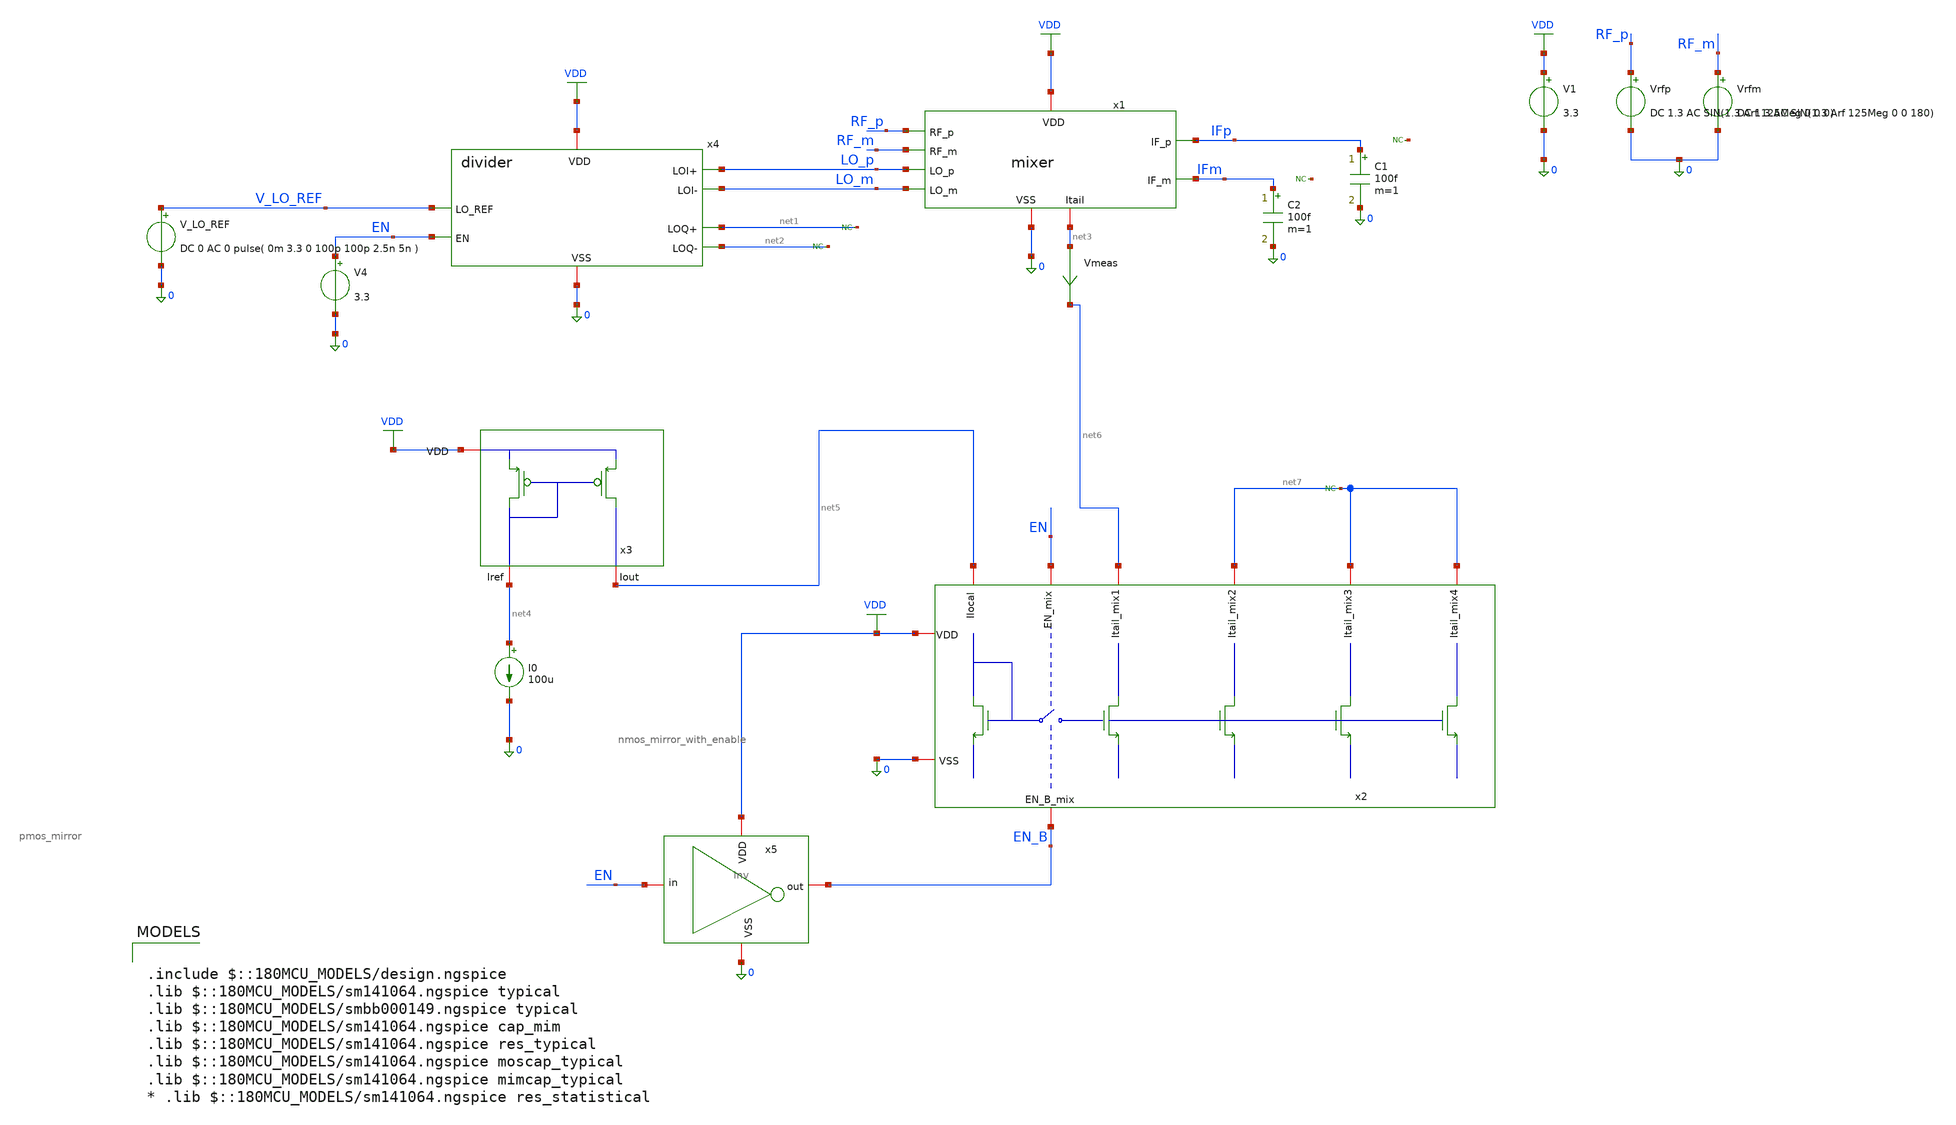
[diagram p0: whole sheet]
** sch_path: designs/mixer/testbench/mixer_p1db.sch
**.subckt mixer_p1db
V1 VDD 0 3.3
Vrfp RF_p 0 DC 1.3 AC SIN(1.3 Arf 125Meg 0 0 0)
Vrfm RF_m 0 DC 1.3 AC SIN(1.3 Arf 125Meg 0 0 180)
C1 IFp 0 100f m=1
C2 IFm 0 100f m=1
x1 IFp RF_p VDD 0 IFm RF_m LO_p net3 LO_m mixer
V_LO_REF V_LO_REF 0 DC 0 AC 0 pulse( 0m 3.3 0 100p 100p 2.5n 5n )
x4 VDD 0 V_LO_REF LO_p LO_m net1 net2 EN divider
* noconn #net1
* noconn #net2
V4 EN 0 3.3
x3 VDD net5 net4 pmos_mirror
I0 net4 0 100u
x2 net7 net7 net5 VDD EN net6 0 EN_B net7 nmos_mirror_with_enable
* noconn #net7
x5 VDD EN_B EN 0 inv
Vmeas net3 net6 0
.save i(vmeas)
* noconn #net8
* noconn #net9
**** begin user architecture code

.include $::180MCU_MODELS/design.ngspice
.lib $::180MCU_MODELS/sm141064.ngspice typical
.lib $::180MCU_MODELS/smbb000149.ngspice typical
.lib $::180MCU_MODELS/sm141064.ngspice cap_mim
.lib $::180MCU_MODELS/sm141064.ngspice res_typical
.lib $::180MCU_MODELS/sm141064.ngspice moscap_typical
.lib $::180MCU_MODELS/sm141064.ngspice mimcap_typical
* .lib $::180MCU_MODELS/sm141064.ngspice res_statistical




.param Arf=10m
.control
op
destroy all
write mixer_p1db.raw

foreach A 25m
alterparam Arf=$A
reset
save v(ifp) v(ifm)
tran 0.01n 2u  ;transient sim

let vif = V(IFp)-V(IFm)


fft vif

plot mag(vif) vs frequency xlimit 0 200Meg
end
.endc


**** end user architecture code
**.ends
.GLOBAL VDD
.end
